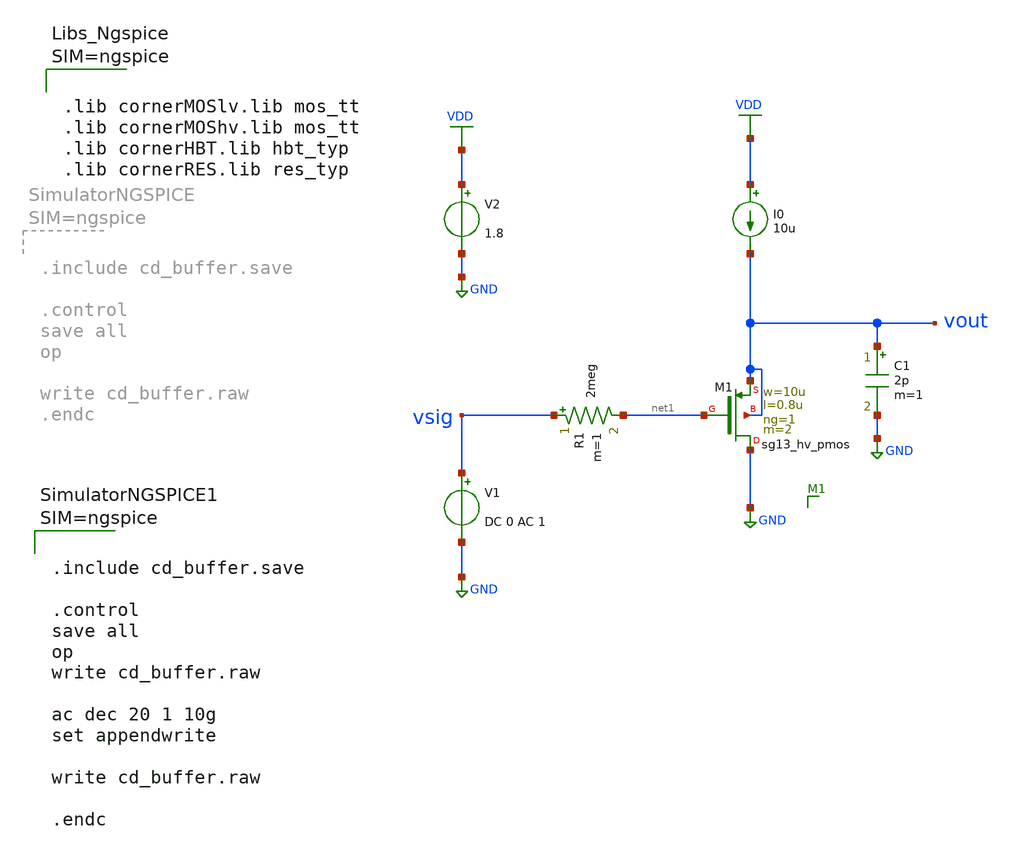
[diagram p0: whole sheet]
** sch_path: Schematics/lab_3/cd_buffer.sch
**.subckt cd_buffer
XM1 GND net1 vout vout sg13_hv_pmos w=10u l=0.8u ng=1 m=2 mm_ok=1
R1 vsig net1 2meg m=1
V1 vsig GND DC 0 AC 1
I0 VDD vout 10u
V2 VDD GND 1.8
C1 vout GND 2p m=1
**** begin user architecture code



.lib cornerMOSlv.lib mos_tt
.lib cornerMOShv.lib mos_tt
.lib cornerHBT.lib hbt_typ
.lib cornerRES.lib res_typ






.include cd_buffer.save

.control
save all
op
write cd_buffer.raw

ac dec 20 1 10g
set appendwrite

write cd_buffer.raw

.endc



**** end user architecture code
**.ends
.GLOBAL GND
.GLOBAL VDD
.end
